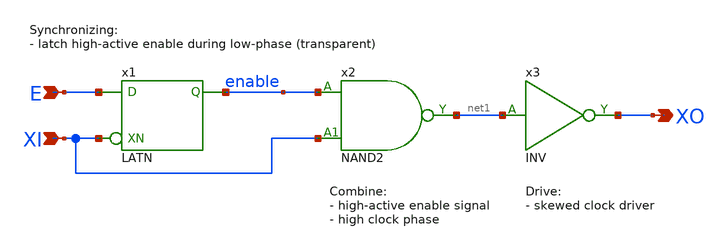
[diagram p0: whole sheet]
** sch_path: Sources/macros/CGP2.sch
**.subckt CGP2 E XI XO
*.ipin E
*.ipin XI
*.opin XO
x1 E XI enable VDD GND LATN Wmin=1.5u Lmin=1u g=2 m=1
x2 enable XI net1 VDD GND NAND2 Wmin=1.5u Lmin=1u g=2 m=1
x3 net1 XO VDD GND INV Wmin=1.5u Lmin=1u g=2 m=1
**.ends
.end
